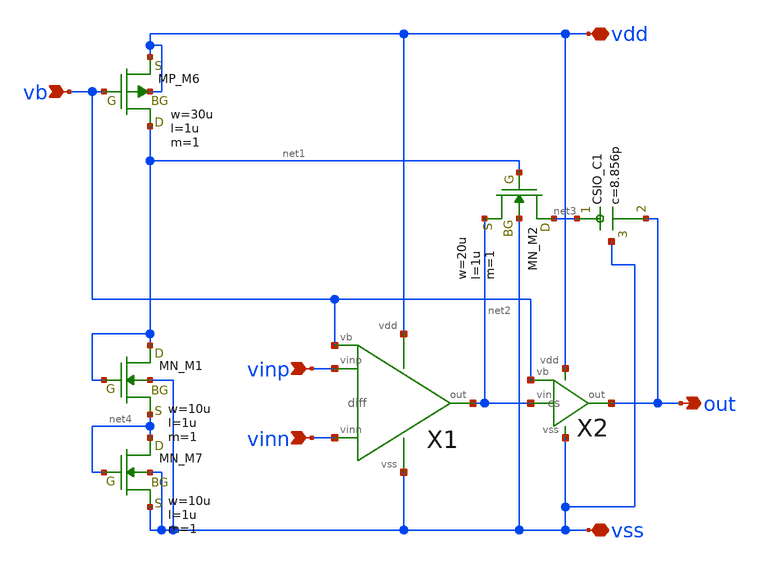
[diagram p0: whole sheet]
** sch_path: OpenSUSI-TR10/opamp/2stage_pc.sch
**.subckt 2stage_pc vinp vinn vb out vdd vss
*.ipin vinp
*.ipin vinn
*.ipin vb
*.opin out
*.iopin vdd
*.iopin vss
X1 vinp vinn net2 vdd vss vb diff
X2 net2 vb out vdd vss cs
XM6 net1 vb vdd vdd PMOS w=30u l=1u as=0 ad=0 ps=0 pd=0 nrd=0 nrs=0 m=1
XM1 net1 net1 net4 vss NMOS w=10u l=1u as=0 ad=0 ps=0 pd=0 nrd=0 nrs=0 m=1
XM7 net4 net4 vss vss NMOS w=10u l=1u as=0 ad=0 ps=0 pd=0 nrd=0 nrs=0 m=1
XM2 net3 net1 net2 vss NMOS w=20u l=1u as=0 ad=0 ps=0 pd=0 nrd=0 nrs=0 m=1
XC1 net3 out vss F_CSIO c=8.856p x=120u y=120u m=1
**.ends

* expanding   symbol:  diff.sym # of pins=6
** sym_path: diff.sym
** sch_path: diff.sch
.subckt diff vinp vinn out vdd vss vb
*.ipin vinn
*.ipin vinp
*.ipin vb
*.opin out
*.iopin vdd
*.iopin vss
M5 net2 vb vdd vdd pmos L=2u W=40u m=1
M1 net1 vinn net2 net2 pmos L=2u W=200u m=1
M2 out vinp net2 net2 pmos L=2u W=200u m=1
M3 net1 net1 vss vss nmos L=2u W=10u m=1
M4 out net1 vss vss nmos L=2u W=10u m=1
.ends


* expanding   symbol:  cs.sym # of pins=5
** sym_path: cs.sym
** sch_path: cs.sch
.subckt cs vin vb out vdd vss
*.ipin vb
*.ipin vin
*.opin out
*.iopin vss
*.iopin vdd
XM6 out vb vdd vdd PMOS w=270u l=1u as=0 ad=0 ps=0 pd=0 nrd=0 nrs=0 m=1
XM7 out vin vss vss NMOS w=90u l=1u as=0 ad=0 ps=0 pd=0 nrd=0 nrs=0 m=1
.ends

.end
